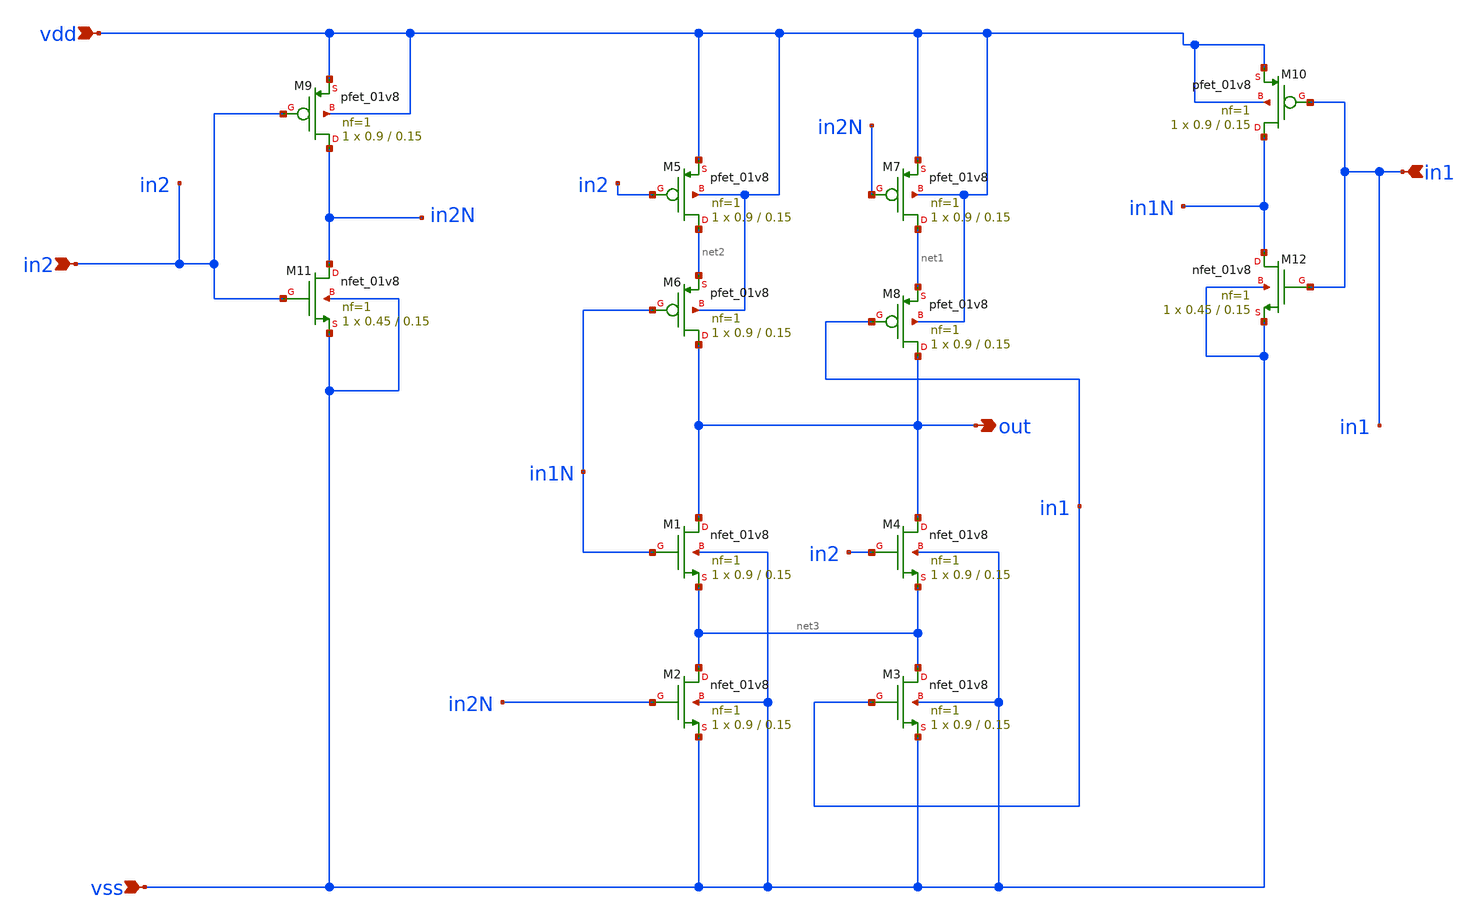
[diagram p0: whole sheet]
** sch_path: track_vlsi/lapi-fernandez/sch/xor.sch
**.subckt xor in1 in2 vss vdd out
*.ipin in1
*.ipin in2
*.ipin vss
*.ipin vdd
*.opin out
XM1 out in1N net3 vss sky130_fd_pr__nfet_01v8 L=0.15 W=0.9 nf=1 ad='int((nf+1)/2) * W/nf * 0.29' as='int((nf+2)/2) * W/nf * 0.29'
+ pd='2*int((nf+1)/2) * (W/nf + 0.29)' ps='2*int((nf+2)/2) * (W/nf + 0.29)' nrd='0.29 / W' nrs='0.29 / W'
+ sa=0 sb=0 sd=0 mult=1 m=1
XM2 net3 in2N vss vss sky130_fd_pr__nfet_01v8 L=0.15 W=0.9 nf=1 ad='int((nf+1)/2) * W/nf * 0.29' as='int((nf+2)/2) * W/nf * 0.29'
+ pd='2*int((nf+1)/2) * (W/nf + 0.29)' ps='2*int((nf+2)/2) * (W/nf + 0.29)' nrd='0.29 / W' nrs='0.29 / W'
+ sa=0 sb=0 sd=0 mult=1 m=1
XM3 net3 in1 vss vss sky130_fd_pr__nfet_01v8 L=0.15 W=0.9 nf=1 ad='int((nf+1)/2) * W/nf * 0.29' as='int((nf+2)/2) * W/nf * 0.29'
+ pd='2*int((nf+1)/2) * (W/nf + 0.29)' ps='2*int((nf+2)/2) * (W/nf + 0.29)' nrd='0.29 / W' nrs='0.29 / W'
+ sa=0 sb=0 sd=0 mult=1 m=1
XM4 out in2 net3 vss sky130_fd_pr__nfet_01v8 L=0.15 W=0.9 nf=1 ad='int((nf+1)/2) * W/nf * 0.29' as='int((nf+2)/2) * W/nf * 0.29'
+ pd='2*int((nf+1)/2) * (W/nf + 0.29)' ps='2*int((nf+2)/2) * (W/nf + 0.29)' nrd='0.29 / W' nrs='0.29 / W'
+ sa=0 sb=0 sd=0 mult=1 m=1
XM5 net2 in2 vdd vdd sky130_fd_pr__pfet_01v8 L=0.15 W=0.9 nf=1 ad='int((nf+1)/2) * W/nf * 0.29' as='int((nf+2)/2) * W/nf * 0.29'
+ pd='2*int((nf+1)/2) * (W/nf + 0.29)' ps='2*int((nf+2)/2) * (W/nf + 0.29)' nrd='0.29 / W' nrs='0.29 / W'
+ sa=0 sb=0 sd=0 mult=1 m=1
XM6 out in1N net2 vdd sky130_fd_pr__pfet_01v8 L=0.15 W=0.9 nf=1 ad='int((nf+1)/2) * W/nf * 0.29' as='int((nf+2)/2) * W/nf * 0.29'
+ pd='2*int((nf+1)/2) * (W/nf + 0.29)' ps='2*int((nf+2)/2) * (W/nf + 0.29)' nrd='0.29 / W' nrs='0.29 / W'
+ sa=0 sb=0 sd=0 mult=1 m=1
XM7 net1 in2N vdd vdd sky130_fd_pr__pfet_01v8 L=0.15 W=0.9 nf=1 ad='int((nf+1)/2) * W/nf * 0.29' as='int((nf+2)/2) * W/nf * 0.29'
+ pd='2*int((nf+1)/2) * (W/nf + 0.29)' ps='2*int((nf+2)/2) * (W/nf + 0.29)' nrd='0.29 / W' nrs='0.29 / W'
+ sa=0 sb=0 sd=0 mult=1 m=1
XM8 out in1 net1 vdd sky130_fd_pr__pfet_01v8 L=0.15 W=0.9 nf=1 ad='int((nf+1)/2) * W/nf * 0.29' as='int((nf+2)/2) * W/nf * 0.29'
+ pd='2*int((nf+1)/2) * (W/nf + 0.29)' ps='2*int((nf+2)/2) * (W/nf + 0.29)' nrd='0.29 / W' nrs='0.29 / W'
+ sa=0 sb=0 sd=0 mult=1 m=1
XM9 in2N in2 vdd vdd sky130_fd_pr__pfet_01v8 L=0.15 W=0.9 nf=1 ad='int((nf+1)/2) * W/nf * 0.29' as='int((nf+2)/2) * W/nf * 0.29'
+ pd='2*int((nf+1)/2) * (W/nf + 0.29)' ps='2*int((nf+2)/2) * (W/nf + 0.29)' nrd='0.29 / W' nrs='0.29 / W'
+ sa=0 sb=0 sd=0 mult=1 m=1
XM10 in1N in1 vdd vdd sky130_fd_pr__pfet_01v8 L=0.15 W=0.9 nf=1 ad='int((nf+1)/2) * W/nf * 0.29' as='int((nf+2)/2) * W/nf * 0.29'
+ pd='2*int((nf+1)/2) * (W/nf + 0.29)' ps='2*int((nf+2)/2) * (W/nf + 0.29)' nrd='0.29 / W' nrs='0.29 / W'
+ sa=0 sb=0 sd=0 mult=1 m=1
XM11 in2N in2 vss vss sky130_fd_pr__nfet_01v8 L=0.15 W=0.45 nf=1 ad='int((nf+1)/2) * W/nf * 0.29' as='int((nf+2)/2) * W/nf * 0.29'
+ pd='2*int((nf+1)/2) * (W/nf + 0.29)' ps='2*int((nf+2)/2) * (W/nf + 0.29)' nrd='0.29 / W' nrs='0.29 / W'
+ sa=0 sb=0 sd=0 mult=1 m=1
XM12 in1N in1 vss vss sky130_fd_pr__nfet_01v8 L=0.15 W=0.45 nf=1 ad='int((nf+1)/2) * W/nf * 0.29' as='int((nf+2)/2) * W/nf * 0.29'
+ pd='2*int((nf+1)/2) * (W/nf + 0.29)' ps='2*int((nf+2)/2) * (W/nf + 0.29)' nrd='0.29 / W' nrs='0.29 / W'
+ sa=0 sb=0 sd=0 mult=1 m=1
**.ends
.end
